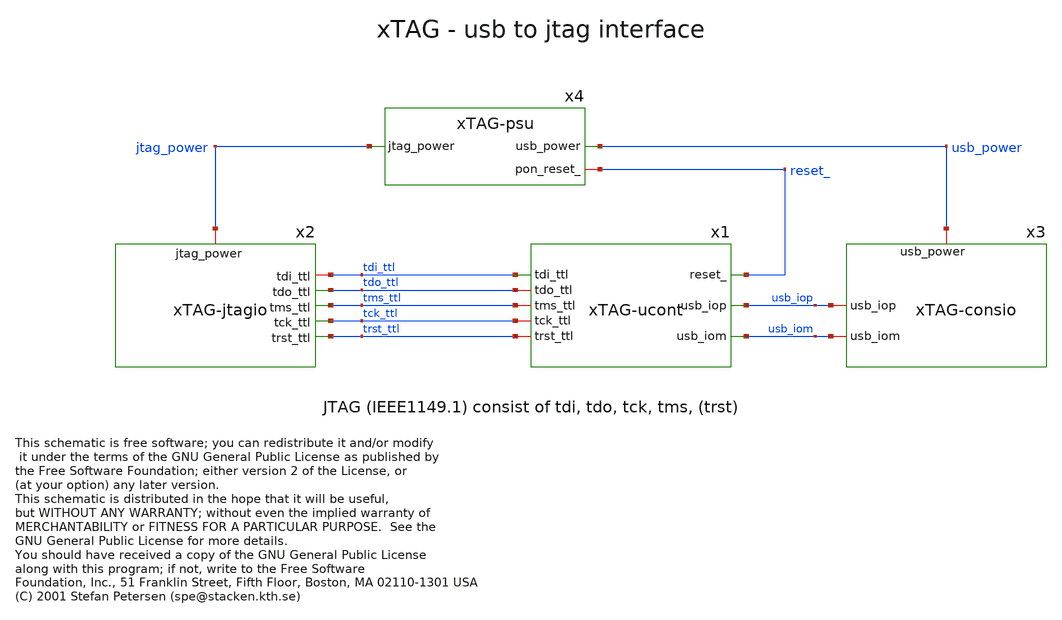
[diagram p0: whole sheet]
** sch_path: xschem_library/xTAG/xTAG.sch
* This schematic is free software; you can redistribute it and/or modify
* it under the terms of the GNU General Public License as published by
* the Free Software Foundation; either version 2 of the License, or
* (at your option) any later version.
* (C) 2001 Stefan Petersen (spe@stacken.kth.se)
**.subckt xTAG
x4 usb_power reset_ jtag_power xTAG-psu
x2 jtag_power tdi_ttl tdo_ttl tms_ttl tck_ttl trst_ttl xTAG-jtagio
x1 tdi_ttl tdo_ttl tms_ttl tck_ttl trst_ttl reset_ usb_iop usb_iom xTAG-ucont
x3 usb_power usb_iop usb_iom xTAG-consio
**.ends
.end
